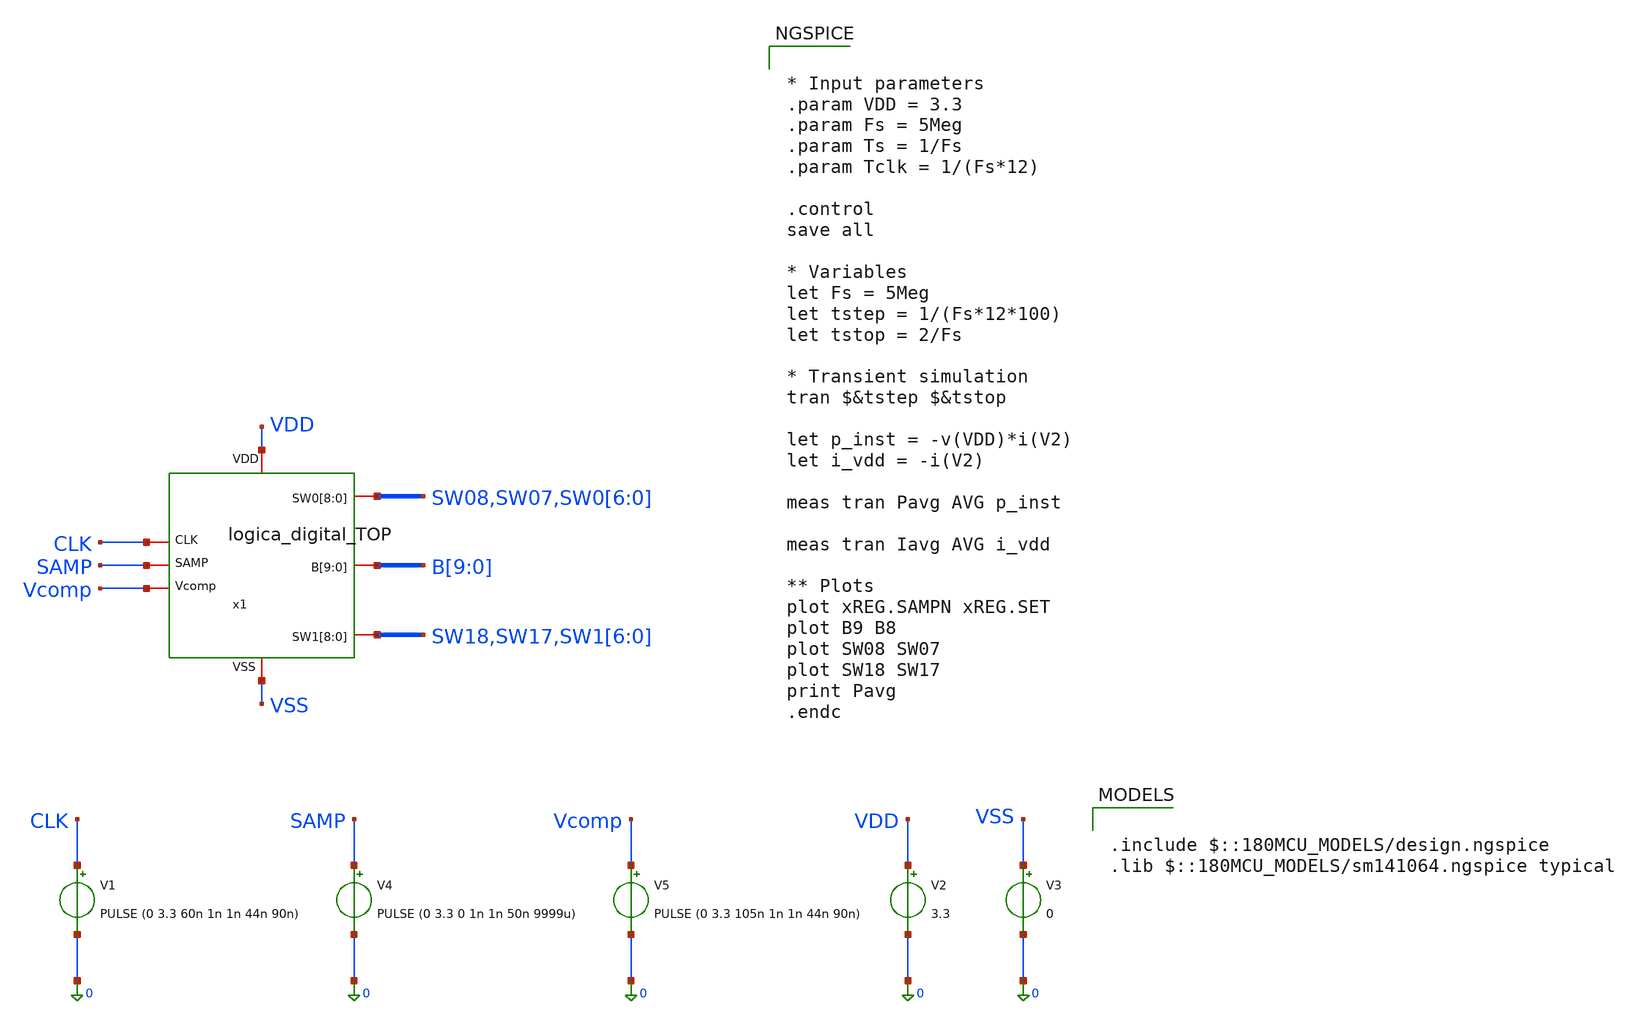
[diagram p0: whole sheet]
** sch_path: designs/sar_adc/digital/logica_digital_TOP/xschem/logica_digital_TOP_tb.sch
**.subckt logica_digital_TOP_tb
V1 CLK 0 PULSE (0 3.3 60n 1n 1n 44n 90n)
V2 VDD 0 3.3
V3 VSS 0 0
V5 Vcomp 0 PULSE (0 3.3 105n 1n 1n 44n 90n)
x1 VDD CLK SAMP Vcomp SW08 SW07 SW0[6] SW0[5] SW0[4] SW0[3] SW0[2] SW0[1] SW0[0] B[9] B[8] B[7] B[6]
+ B[5] B[4] B[3] B[2] B[1] B[0] SW18 SW17 SW1[6] SW1[5] SW1[4] SW1[3] SW1[2] SW1[1] SW1[0] VSS
+ logica_digital_TOP
V4 SAMP 0 PULSE (0 3.3 0 1n 1n 50n 9999u)
**** begin user architecture code


* Input parameters
.param VDD = 3.3
.param Fs = 5Meg
.param Ts = 1/Fs
.param Tclk = 1/(Fs*12)

.control
save all

* Variables
let Fs = 5Meg
let tstep = 1/(Fs*12*100)
let tstop = 2/Fs

* Transient simulation
tran $&tstep $&tstop

let p_inst = -v(VDD)*i(V2)
let i_vdd = -i(V2)

meas tran Pavg AVG p_inst

meas tran Iavg AVG i_vdd

** Plots
plot xREG.SAMPN xREG.SET
plot B9 B8
plot SW08 SW07
plot SW18 SW17
print Pavg
.endc



.include $::180MCU_MODELS/design.ngspice
.lib $::180MCU_MODELS/sm141064.ngspice typical

**** end user architecture code
**.ends
.end
